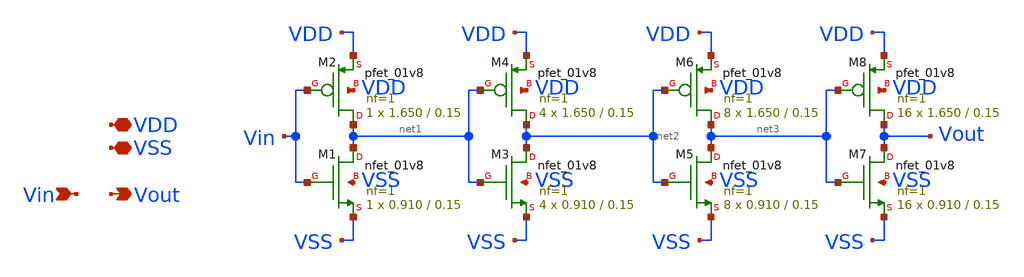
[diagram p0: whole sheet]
** sch_path: xschem/src/capacitor_switch16/capacitor_switch16.sch
**.subckt capacitor_switch16 VDD Vin Vout VSS
*.iopin VDD
*.ipin Vin
*.opin Vout
*.iopin VSS
XM1 net1 Vin VSS VSS sky130_fd_pr__nfet_01v8 L=0.15 W=0.910 nf=1 ad='int((nf+1)/2) * W/nf * 0.29' as='int((nf+2)/2) * W/nf * 0.29'
+ pd='2*int((nf+1)/2) * (W/nf + 0.29)' ps='2*int((nf+2)/2) * (W/nf + 0.29)' nrd='0.29 / W' nrs='0.29 / W'
+ sa=0 sb=0 sd=0 mult=1 m=1
XM2 net1 Vin VDD VDD sky130_fd_pr__pfet_01v8 L=0.15 W=1.650 nf=1 ad='int((nf+1)/2) * W/nf * 0.29' as='int((nf+2)/2) * W/nf * 0.29'
+ pd='2*int((nf+1)/2) * (W/nf + 0.29)' ps='2*int((nf+2)/2) * (W/nf + 0.29)' nrd='0.29 / W' nrs='0.29 / W'
+ sa=0 sb=0 sd=0 mult=1 m=1
XM3 net2 net1 VSS VSS sky130_fd_pr__nfet_01v8 L=0.15 W=0.910 nf=1 ad='int((nf+1)/2) * W/nf * 0.29' as='int((nf+2)/2) * W/nf * 0.29'
+ pd='2*int((nf+1)/2) * (W/nf + 0.29)' ps='2*int((nf+2)/2) * (W/nf + 0.29)' nrd='0.29 / W' nrs='0.29 / W'
+ sa=0 sb=0 sd=0 mult=4 m=4
XM4 net2 net1 VDD VDD sky130_fd_pr__pfet_01v8 L=0.15 W=1.650 nf=1 ad='int((nf+1)/2) * W/nf * 0.29' as='int((nf+2)/2) * W/nf * 0.29'
+ pd='2*int((nf+1)/2) * (W/nf + 0.29)' ps='2*int((nf+2)/2) * (W/nf + 0.29)' nrd='0.29 / W' nrs='0.29 / W'
+ sa=0 sb=0 sd=0 mult=4 m=4
XM5 net3 net2 VSS VSS sky130_fd_pr__nfet_01v8 L=0.15 W=0.910 nf=1 ad='int((nf+1)/2) * W/nf * 0.29' as='int((nf+2)/2) * W/nf * 0.29'
+ pd='2*int((nf+1)/2) * (W/nf + 0.29)' ps='2*int((nf+2)/2) * (W/nf + 0.29)' nrd='0.29 / W' nrs='0.29 / W'
+ sa=0 sb=0 sd=0 mult=8 m=8
XM6 net3 net2 VDD VDD sky130_fd_pr__pfet_01v8 L=0.15 W=1.650 nf=1 ad='int((nf+1)/2) * W/nf * 0.29' as='int((nf+2)/2) * W/nf * 0.29'
+ pd='2*int((nf+1)/2) * (W/nf + 0.29)' ps='2*int((nf+2)/2) * (W/nf + 0.29)' nrd='0.29 / W' nrs='0.29 / W'
+ sa=0 sb=0 sd=0 mult=8 m=8
XM7 Vout net3 VSS VSS sky130_fd_pr__nfet_01v8 L=0.15 W=0.910 nf=1 ad='int((nf+1)/2) * W/nf * 0.29' as='int((nf+2)/2) * W/nf * 0.29'
+ pd='2*int((nf+1)/2) * (W/nf + 0.29)' ps='2*int((nf+2)/2) * (W/nf + 0.29)' nrd='0.29 / W' nrs='0.29 / W'
+ sa=0 sb=0 sd=0 mult=16 m=16
XM8 Vout net3 VDD VDD sky130_fd_pr__pfet_01v8 L=0.15 W=1.650 nf=1 ad='int((nf+1)/2) * W/nf * 0.29' as='int((nf+2)/2) * W/nf * 0.29'
+ pd='2*int((nf+1)/2) * (W/nf + 0.29)' ps='2*int((nf+2)/2) * (W/nf + 0.29)' nrd='0.29 / W' nrs='0.29 / W'
+ sa=0 sb=0 sd=0 mult=16 m=16
**.ends
.end
